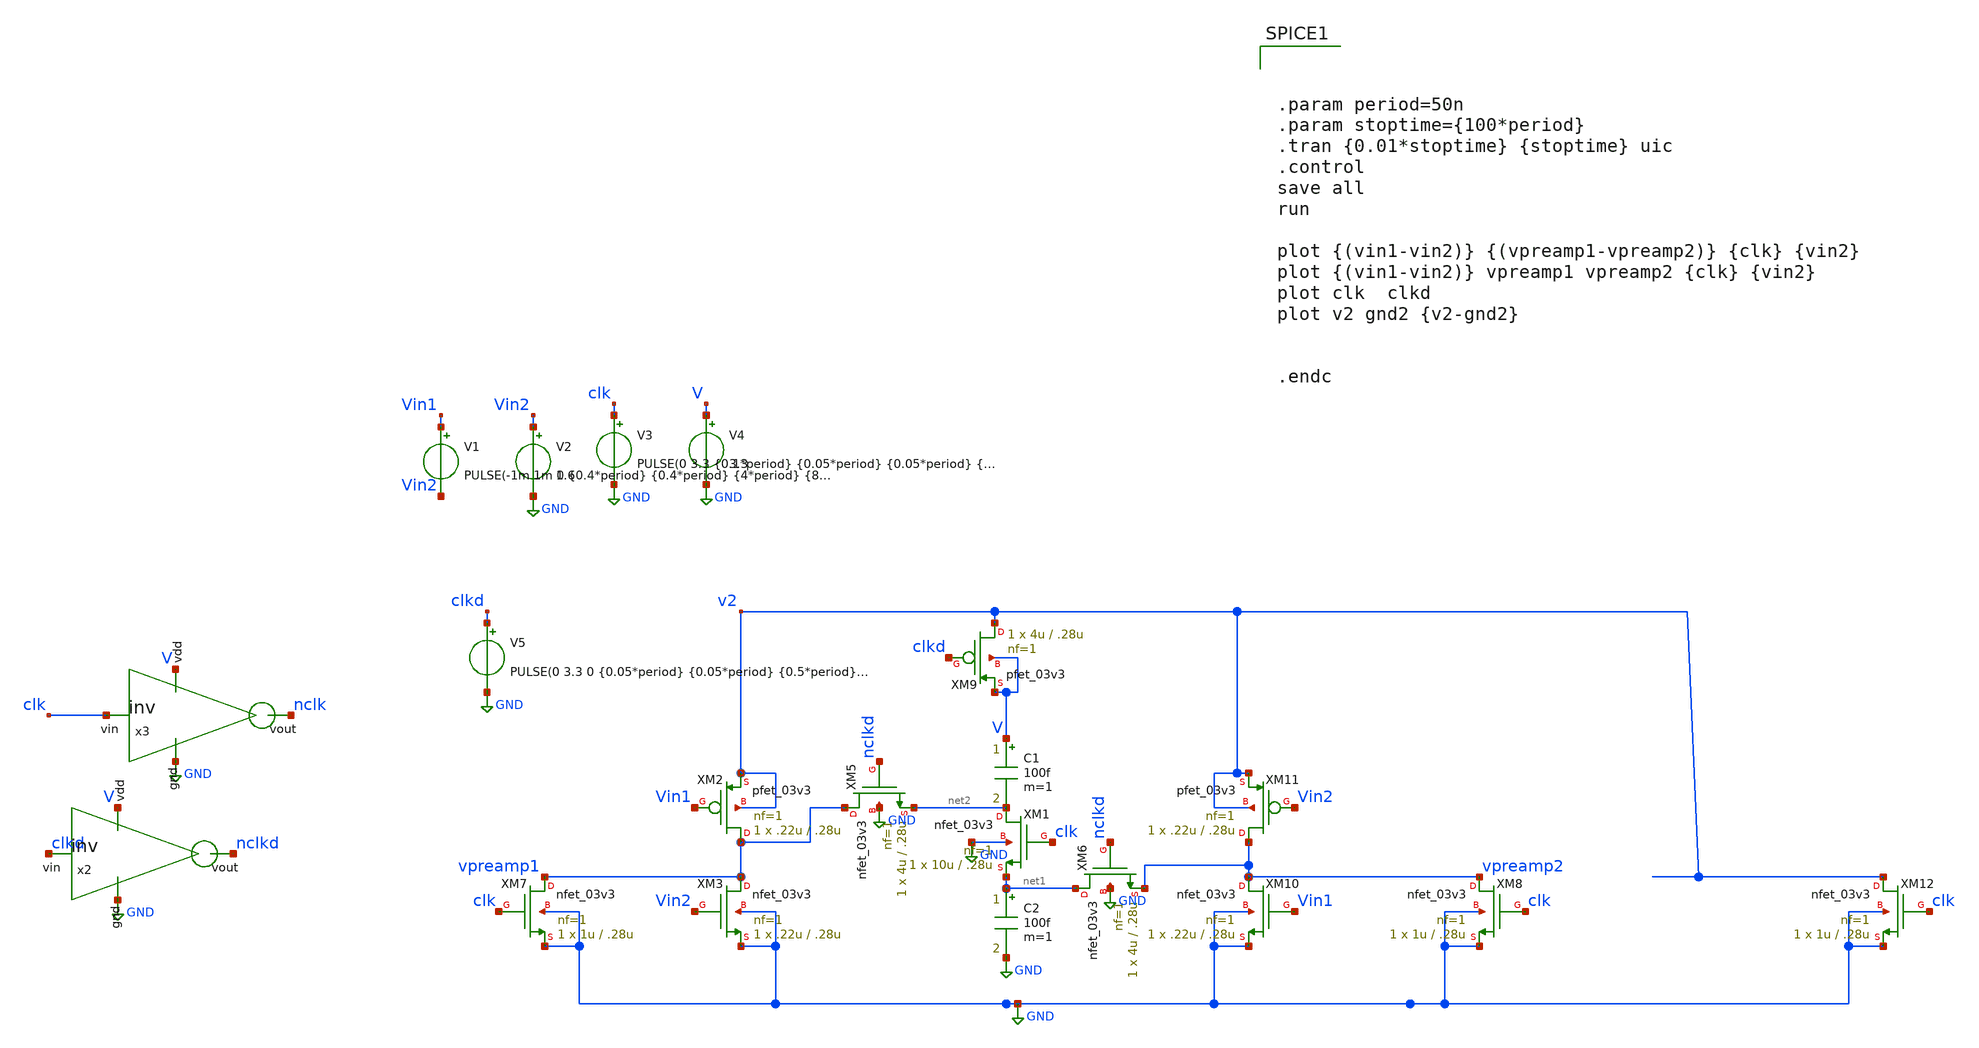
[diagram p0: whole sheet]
** sch_path: xschem/test/comp_full_tb/comp_step_tb.sch
**.subckt comp_step_tb
V3 clk GND PULSE(0 3.3 {0.1*period} {0.05*period} {0.05*period} {0.3*period} {1*period})
V4 V GND 3.3
x3 V GND nclk clk inv cl=0.28u wp=0.44u wn=0.22u wx=.22u mx=1
XM9 v2 clkd V V pfet_03v3 L=.28u W=4u nf=1 ad='int((nf+1)/2) * W/nf * 0.18u' as='int((nf+2)/2) * W/nf * 0.18u'
+ pd='2*int((nf+1)/2) * (W/nf + 0.18u)' ps='2*int((nf+2)/2) * (W/nf + 0.18u)' nrd='0.18u / W' nrs='0.18u / W'
+ sa=0 sb=0 sd=0 m=1
XM11 vpreamp2 Vin2 v2 v2 pfet_03v3 L=.28u W=.22u nf=1 ad='int((nf+1)/2) * W/nf * 0.18u' as='int((nf+2)/2) * W/nf * 0.18u'
+ pd='2*int((nf+1)/2) * (W/nf + 0.18u)' ps='2*int((nf+2)/2) * (W/nf + 0.18u)' nrd='0.18u / W' nrs='0.18u / W'
+ sa=0 sb=0 sd=0 m=1
C1 V net2 100f m=1
C2 net1 GND 100f m=1
V1 Vin1 Vin2 PULSE(-1m 1m 0 {0.4*period} {0.4*period} {4*period} {8*period})
V2 Vin2 GND 1.6
XM10 vpreamp2 Vin1 GND GND nfet_03v3 L=.28u W=.22u nf=1 ad='int((nf+1)/2) * W/nf * 0.18u' as='int((nf+2)/2) * W/nf * 0.18u'
+ pd='2*int((nf+1)/2) * (W/nf + 0.18u)' ps='2*int((nf+2)/2) * (W/nf + 0.18u)' nrd='0.18u / W' nrs='0.18u / W'
+ sa=0 sb=0 sd=0 m=1
XM1 net2 clk net1 GND nfet_03v3 L=.28u W=10u nf=1 ad='int((nf+1)/2) * W/nf * 0.18u' as='int((nf+2)/2) * W/nf * 0.18u'
+ pd='2*int((nf+1)/2) * (W/nf + 0.18u)' ps='2*int((nf+2)/2) * (W/nf + 0.18u)' nrd='0.18u / W' nrs='0.18u / W'
+ sa=0 sb=0 sd=0 m=1
XM2 vpreamp1 Vin1 v2 v2 pfet_03v3 L=.28u W=.22u nf=1 ad='int((nf+1)/2) * W/nf * 0.18u' as='int((nf+2)/2) * W/nf * 0.18u'
+ pd='2*int((nf+1)/2) * (W/nf + 0.18u)' ps='2*int((nf+2)/2) * (W/nf + 0.18u)' nrd='0.18u / W' nrs='0.18u / W'
+ sa=0 sb=0 sd=0 m=1
XM3 vpreamp1 Vin2 GND GND nfet_03v3 L=.28u W=.22u nf=1 ad='int((nf+1)/2) * W/nf * 0.18u' as='int((nf+2)/2) * W/nf * 0.18u'
+ pd='2*int((nf+1)/2) * (W/nf + 0.18u)' ps='2*int((nf+2)/2) * (W/nf + 0.18u)' nrd='0.18u / W' nrs='0.18u / W'
+ sa=0 sb=0 sd=0 m=1
x2 V GND nclkd clkd inv cl=0.28u wp=0.44u wn=0.22u wx=10u mx=1
V5 clkd GND PULSE(0 3.3 0 {0.05*period} {0.05*period} {0.5*period} {1*period})
XM6 net1 nclkd vpreamp2 GND nfet_03v3 L=.28u W=4u nf=1 ad='int((nf+1)/2) * W/nf * 0.18u' as='int((nf+2)/2) * W/nf * 0.18u'
+ pd='2*int((nf+1)/2) * (W/nf + 0.18u)' ps='2*int((nf+2)/2) * (W/nf + 0.18u)' nrd='0.18u / W' nrs='0.18u / W'
+ sa=0 sb=0 sd=0 m=1
XM5 vpreamp1 nclkd net2 GND nfet_03v3 L=.28u W=4u nf=1 ad='int((nf+1)/2) * W/nf * 0.18u' as='int((nf+2)/2) * W/nf * 0.18u'
+ pd='2*int((nf+1)/2) * (W/nf + 0.18u)' ps='2*int((nf+2)/2) * (W/nf + 0.18u)' nrd='0.18u / W' nrs='0.18u / W'
+ sa=0 sb=0 sd=0 m=1
XM7 vpreamp1 clk GND GND nfet_03v3 L=.28u W=1u nf=1 ad='int((nf+1)/2) * W/nf * 0.18u' as='int((nf+2)/2) * W/nf * 0.18u'
+ pd='2*int((nf+1)/2) * (W/nf + 0.18u)' ps='2*int((nf+2)/2) * (W/nf + 0.18u)' nrd='0.18u / W' nrs='0.18u / W'
+ sa=0 sb=0 sd=0 m=1
XM8 vpreamp2 clk GND GND nfet_03v3 L=.28u W=1u nf=1 ad='int((nf+1)/2) * W/nf * 0.18u' as='int((nf+2)/2) * W/nf * 0.18u'
+ pd='2*int((nf+1)/2) * (W/nf + 0.18u)' ps='2*int((nf+2)/2) * (W/nf + 0.18u)' nrd='0.18u / W' nrs='0.18u / W'
+ sa=0 sb=0 sd=0 m=1
XM12 v2 clk GND GND nfet_03v3 L=.28u W=1u nf=1 ad='int((nf+1)/2) * W/nf * 0.18u' as='int((nf+2)/2) * W/nf * 0.18u'
+ pd='2*int((nf+1)/2) * (W/nf + 0.18u)' ps='2*int((nf+2)/2) * (W/nf + 0.18u)' nrd='0.18u / W' nrs='0.18u / W'
+ sa=0 sb=0 sd=0 m=1
**** begin user architecture code



.param period=50n
.param stoptime={100*period}
.tran {0.01*stoptime} {stoptime} uic
.control
save all
run

plot {(vin1-vin2)} {(vpreamp1-vpreamp2)} {clk} {vin2}
plot {(vin1-vin2)} vpreamp1 vpreamp2 {clk} {vin2}
plot clk  clkd
plot v2 gnd2 {v2-gnd2}


.endc


.include $env(PDK_ROOT)/$env(PDK)/libs.tech/ngspice/design.ngspice
.lib $env(PDK_ROOT)/$env(PDK)/libs.tech/ngspice/sm141064.ngspice typical

**** end user architecture code
**.ends

* expanding   symbol:  inv.sym # of pins=4
** sym_path: xschem/designs/inv.sym
** sch_path: xschem/designs/inv.sch
.subckt inv vdd gnd vout vin  cl=0.28u wp=0.44u wn=0.22u wx=0.22u mx=1
*.ipin gnd
*.ipin vdd
*.ipin vin
*.opin vout
XM1 gnd vin vout gnd nfet_03v3 L=0.28u W=Wx nf=1 ad='int((nf+1)/2) * W/nf * 0.18u' as='int((nf+2)/2) * W/nf * 0.18u'
+ pd='2*int((nf+1)/2) * (W/nf + 0.18u)' ps='2*int((nf+2)/2) * (W/nf + 0.18u)' nrd='0.18u / W' nrs='0.18u / W'
+ sa=0 sb=0 sd=0 m=1
XM2 vdd vin vout vdd pfet_03v3 L=0.28u W=Wx nf=1 ad='int((nf+1)/2) * W/nf * 0.18u' as='int((nf+2)/2) * W/nf * 0.18u'
+ pd='2*int((nf+1)/2) * (W/nf + 0.18u)' ps='2*int((nf+2)/2) * (W/nf + 0.18u)' nrd='0.18u / W' nrs='0.18u / W'
+ sa=0 sb=0 sd=0 m=1
.ends

.GLOBAL GND
.end
